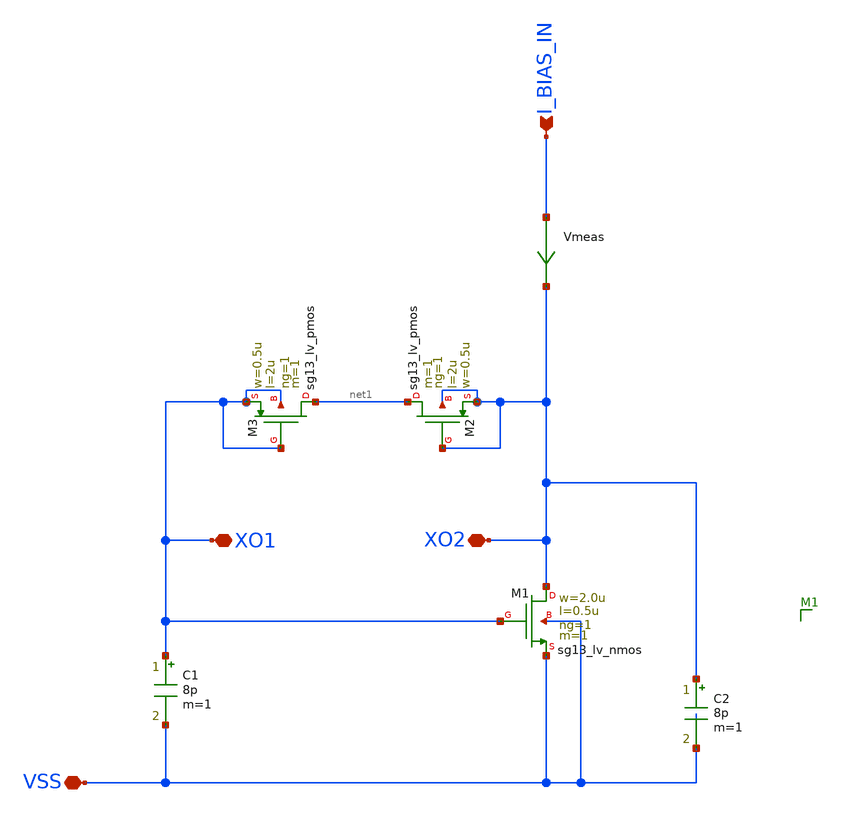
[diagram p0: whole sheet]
** sch_path: xo_core.sch
**.subckt xo_core VSS I_BIAS_IN XO1 XO2
*.iopin VSS
*.ipin I_BIAS_IN
*.iopin XO1
*.iopin XO2
XM2 net1 XO2 XO2 XO2 sg13_lv_pmos w=0.5u l=2u ng=1 m=1 mm_ok=1
XM3 net1 XO1 XO1 XO1 sg13_lv_pmos w=0.5u l=2u ng=1 m=1 mm_ok=1
XM1 XO2 XO1 VSS VSS sg13_lv_nmos w=2.0u l=0.5u ng=1 m=1 mm_ok=1
C2 XO2 VSS 8p m=1
C1 XO1 VSS 8p m=1
Vmeas I_BIAS_IN XO2 0
.save i(vmeas)
**.ends
.end
